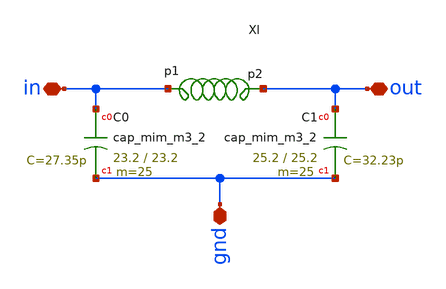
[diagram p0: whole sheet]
** sch_path: impedance-transformer/xschem/impedance-transformer.sch
**.subckt impedance-transformer gnd in out
*.iopin gnd
*.iopin in
*.iopin out
XC0 in gnd sky130_fd_pr__cap_mim_m3_2 W=23.2 L=23.2 MF=25 m=25
XC1 out gnd sky130_fd_pr__cap_mim_m3_2 W=25.2 L=25.2 MF=25 m=25
x1 in out l1
**** begin user architecture code

* NGSPICE file created from impedance-transformer.ext - technology: sky





**** end user architecture code
**.ends

* expanding   symbol:  /home/hugodg/projects-sky130/temp-sensor/impedance-transformer/xschem/l1.sym
*+ # of pins=2
** sym_path: impedance-transformer/xschem/l1.sym
** sch_path: impedance-transformer/xschem/l1.sch
.subckt l1 p1 p2
*.iopin p2
*.iopin p1
L0 p1 net3 275p m=1
Cs1 p1 net1 28.66f m=1
Cs2 p2 net2 25.69f m=1
Rs1 net1 GND 55.23 m=1
Rs2 net2 GND 26 m=1
R1 p2 net3 1.379 m=1
.ends

.GLOBAL GND
.end
